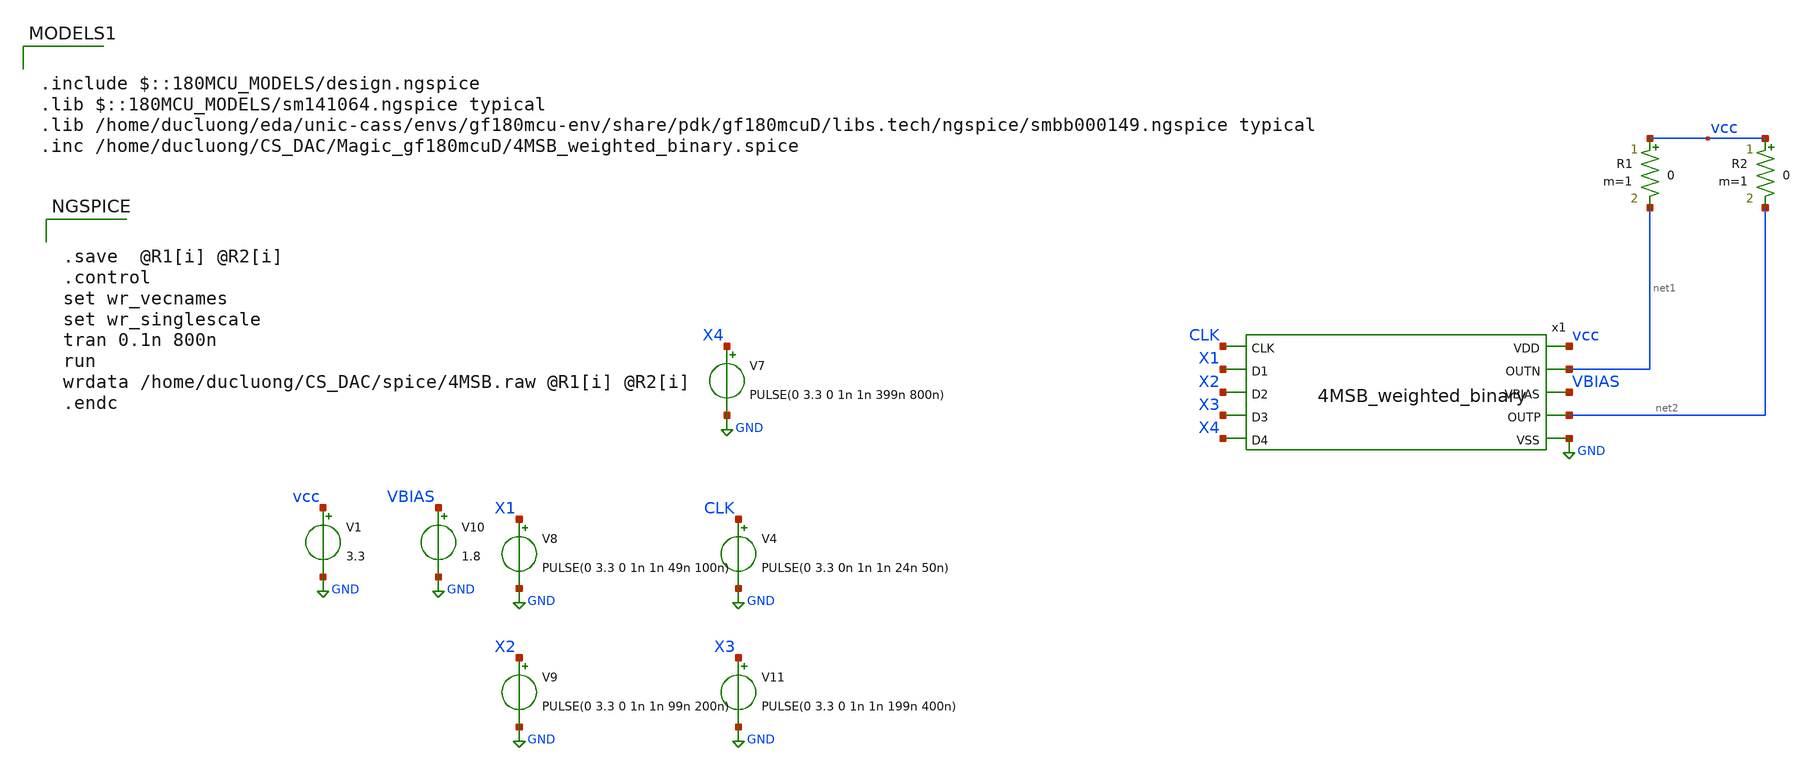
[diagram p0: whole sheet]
** sch_path: xschem/CS.sch
**.subckt CS
V1 vcc GND 3.3
V10 VBIAS GND 1.8
R1 vcc net1 0 m=1
R2 vcc net2 0 m=1
x1 X1 X2 X3 X4 net2 net1 VBIAS CLK vcc GND 4MSB_weighted_binary
V4 CLK GND PULSE(0 3.3 0n 1n 1n 24n 50n)
V8 X1 GND PULSE(0 3.3 0 1n 1n 49n 100n)
V9 X2 GND PULSE(0 3.3 0 1n 1n 99n 200n)
V11 X3 GND PULSE(0 3.3 0 1n 1n 199n 400n)
V7 X4 GND PULSE(0 3.3 0 1n 1n 399n 800n)
**** begin user architecture code

.include $::180MCU_MODELS/design.ngspice
.lib $::180MCU_MODELS/sm141064.ngspice typical
.lib /home/ducluong/eda/unic-cass/envs/gf180mcu-env/share/pdk/gf180mcuD/libs.tech/ngspice/smbb000149.ngspice typical
.inc /home/ducluong/CS_DAC/Magic_gf180mcuD/4MSB_weighted_binary.spice



.save  @R1[i] @R2[i]
.control
set wr_vecnames
set wr_singlescale
tran 0.1n 800n
run
wrdata /home/ducluong/CS_DAC/spice/4MSB.raw @R1[i] @R2[i]
.endc


**** end user architecture code
**.ends
.GLOBAL GND
.end
